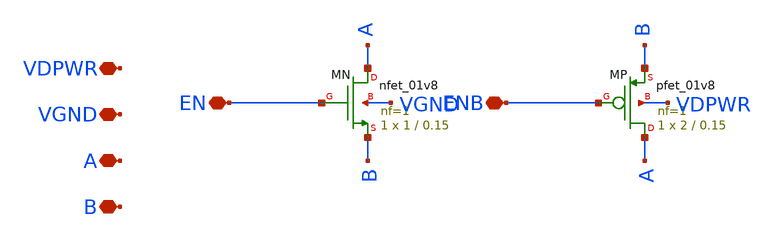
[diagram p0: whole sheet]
** sch_path: cells/ELAD1_TGB/schematic/ELAD1_TGB.sch
**.subckt ELAD1_TGB A B EN ENB VDPWR VGND
*.iopin A
*.iopin B
*.iopin EN
*.iopin ENB
*.iopin VDPWR
*.iopin VGND
XMN A EN B VGND sky130_fd_pr__nfet_01v8 L=0.15 W=1 nf=1 ad='int((1 + 1)/2) * 1 / 1 * 0.29' as='int((1 + 2)/2) * 1 / 1 * 0.29'
+ pd='2*int((1 + 1)/2) * (1 / 1 + 0.29)' ps='2*int((1 + 2)/2) * (1 / 1 + 0.29)' nrd='0.29 / 1 ' nrs='0.29 / 1 '
+ sa=0 sb=0 sd=0 mult=1 m=1
XMP A ENB B VDPWR sky130_fd_pr__pfet_01v8 L=0.15 W=2 nf=1 ad='int((nf+1)/2) * W/nf * 0.29' as='int((nf+2)/2) * W/nf * 0.29'
+ pd='2*int((nf+1)/2) * (W/nf + 0.29)' ps='2*int((nf+2)/2) * (W/nf + 0.29)' nrd='0.29 / W' nrs='0.29 / W'
+ sa=0 sb=0 sd=0 mult=1 m=1
**.ends
.end
